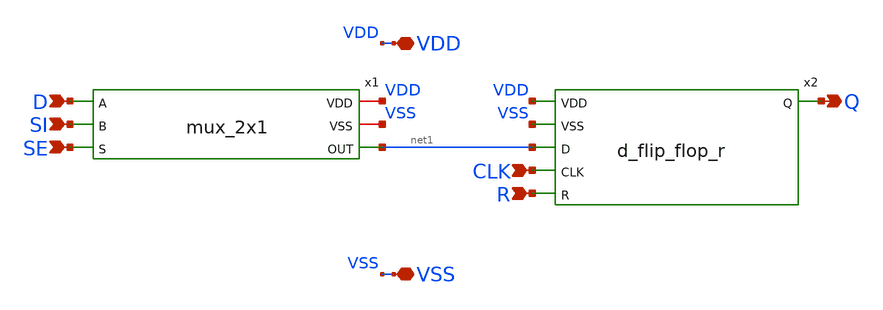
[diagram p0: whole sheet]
** sch_path: designs/cells/sdffrnq/sch/sdffrq.sch
**.subckt sdffrq D SI SE VDD VSS Q R CLK
*.ipin D
*.ipin SI
*.ipin SE
*.iopin VDD
*.iopin VSS
*.opin Q
*.ipin R
*.ipin CLK
x1 D SI VDD VSS SE net1 mux_2x1
x2 VDD VSS Q net1 CLK R d_flip_flop_r
**.ends
.end
